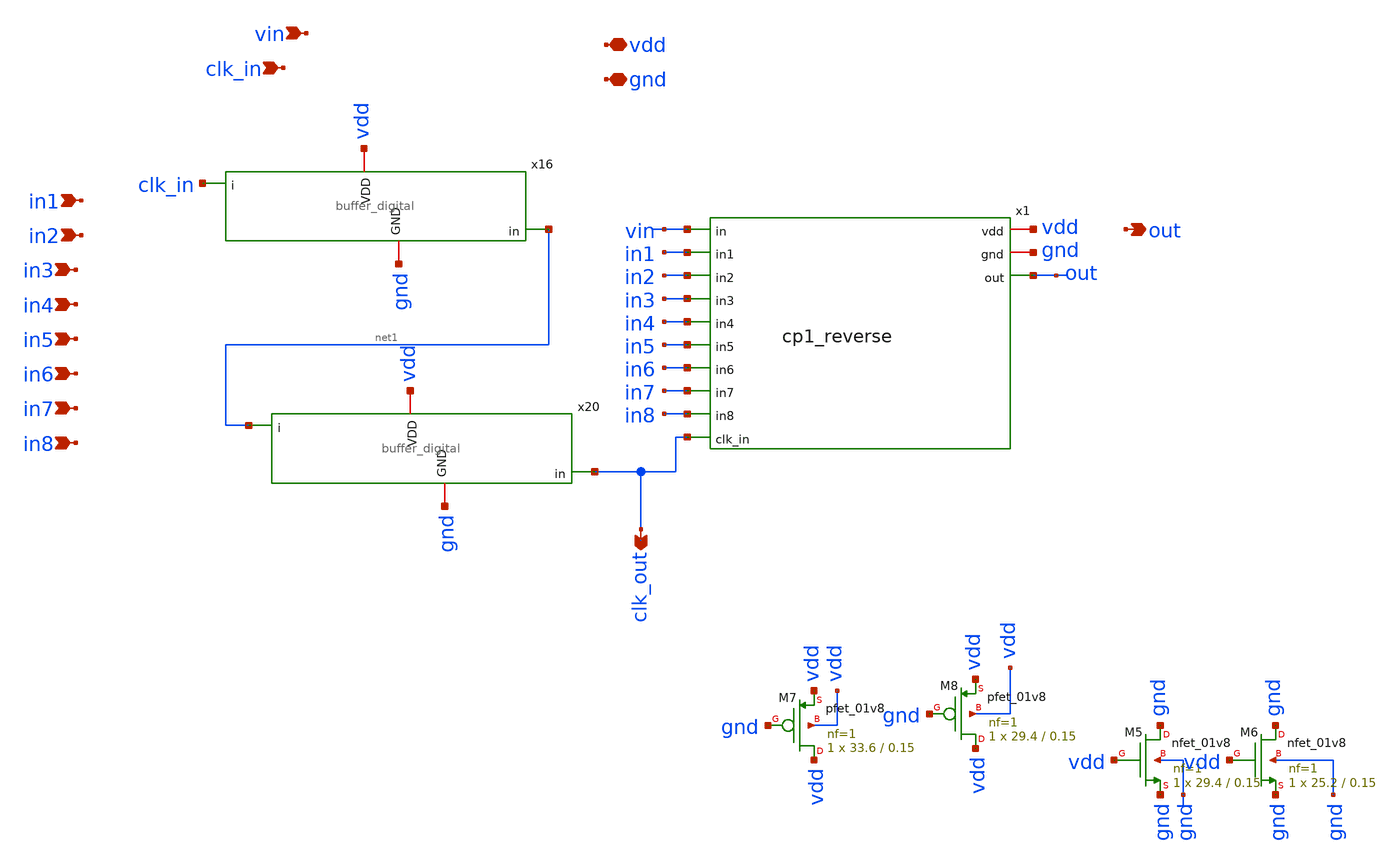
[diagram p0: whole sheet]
** sch_path: xschem/cp1_buffer_reverse.sch
**.subckt cp1_buffer_reverse gnd vdd vin out clk_in in1 in2 in3 in4 in5 in6 in7 in8 clk_out
*.iopin gnd
*.iopin vdd
*.ipin vin
*.opin out
*.ipin clk_in
*.ipin in1
*.ipin in2
*.ipin in3
*.ipin in4
*.ipin in5
*.ipin in6
*.ipin in7
*.ipin in8
*.opin clk_out
x1 vin vdd gnd in1 in2 in3 in4 in5 in6 in7 in8 clk_out out cp1_reverse
x16 gnd vdd clk_in net1 buffer_digital
x20 gnd vdd net1 clk_out buffer_digital
XM5 gnd vdd gnd gnd sky130_fd_pr__nfet_01v8 L=0.15 W=29.4 nf=1 ad='int((nf+1)/2) * W/nf * 0.29' as='int((nf+2)/2) * W/nf * 0.29'
+ pd='2*int((nf+1)/2) * (W/nf + 0.29)' ps='2*int((nf+2)/2) * (W/nf + 0.29)' nrd='0.29 / W' nrs='0.29 / W'
+ sa=0 sb=0 sd=0 mult=1 m=1
XM6 gnd vdd gnd gnd sky130_fd_pr__nfet_01v8 L=0.15 W=25.2 nf=1 ad='int((nf+1)/2) * W/nf * 0.29' as='int((nf+2)/2) * W/nf * 0.29'
+ pd='2*int((nf+1)/2) * (W/nf + 0.29)' ps='2*int((nf+2)/2) * (W/nf + 0.29)' nrd='0.29 / W' nrs='0.29 / W'
+ sa=0 sb=0 sd=0 mult=1 m=1
XM7 vdd gnd vdd vdd sky130_fd_pr__pfet_01v8 L=0.15 W=33.6 nf=1 ad='int((nf+1)/2) * W/nf * 0.29' as='int((nf+2)/2) * W/nf * 0.29'
+ pd='2*int((nf+1)/2) * (W/nf + 0.29)' ps='2*int((nf+2)/2) * (W/nf + 0.29)' nrd='0.29 / W' nrs='0.29 / W'
+ sa=0 sb=0 sd=0 mult=1 m=1
XM8 vdd gnd vdd vdd sky130_fd_pr__pfet_01v8 L=0.15 W=29.4 nf=1 ad='int((nf+1)/2) * W/nf * 0.29' as='int((nf+2)/2) * W/nf * 0.29'
+ pd='2*int((nf+1)/2) * (W/nf + 0.29)' ps='2*int((nf+2)/2) * (W/nf + 0.29)' nrd='0.29 / W' nrs='0.29 / W'
+ sa=0 sb=0 sd=0 mult=1 m=1
**.ends
.end
